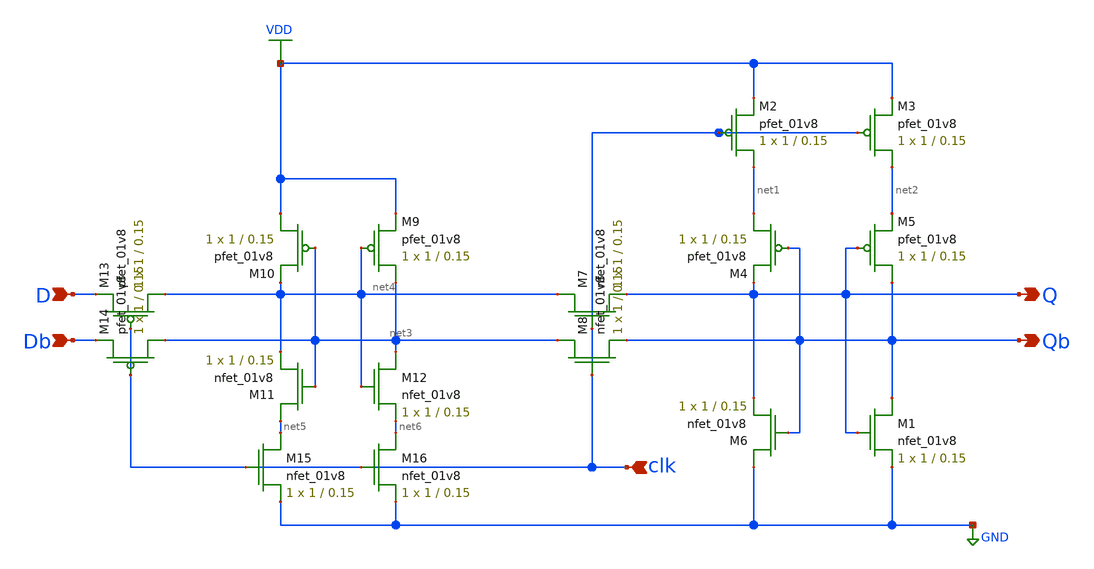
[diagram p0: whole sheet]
** sch_path: Miniproject2/dflipflop_lvs.sch
**.subckt dflipflop_lvs Q Db Qb D clk
*.opin Q
*.ipin Db
*.opin Qb
*.ipin D
*.ipin clk
XM1 Qb Q GND GND sky130_fd_pr__nfet_01v8 L=0.15 W=1 nf=1 ad='int((nf+1)/2) * W/nf * 0.29' as='int((nf+2)/2) * W/nf * 0.29'
+ pd='2*int((nf+1)/2) * (W/nf + 0.29)' ps='2*int((nf+2)/2) * (W/nf + 0.29)' nrd='0.29 / W' nrs='0.29 / W'
+ sa=0 sb=0 sd=0 mult=1 m=1
XM2 net1 clk VDD VDD sky130_fd_pr__pfet_01v8 L=0.15 W=1 nf=1 ad='int((nf+1)/2) * W/nf * 0.29' as='int((nf+2)/2) * W/nf * 0.29'
+ pd='2*int((nf+1)/2) * (W/nf + 0.29)' ps='2*int((nf+2)/2) * (W/nf + 0.29)' nrd='0.29 / W' nrs='0.29 / W'
+ sa=0 sb=0 sd=0 mult=1 m=1
XM3 net2 clk VDD VDD sky130_fd_pr__pfet_01v8 L=0.15 W=1 nf=1 ad='int((nf+1)/2) * W/nf * 0.29' as='int((nf+2)/2) * W/nf * 0.29'
+ pd='2*int((nf+1)/2) * (W/nf + 0.29)' ps='2*int((nf+2)/2) * (W/nf + 0.29)' nrd='0.29 / W' nrs='0.29 / W'
+ sa=0 sb=0 sd=0 mult=1 m=1
XM4 net1 Qb Q VDD sky130_fd_pr__pfet_01v8 L=0.15 W=1 nf=1 ad='int((nf+1)/2) * W/nf * 0.29' as='int((nf+2)/2) * W/nf * 0.29'
+ pd='2*int((nf+1)/2) * (W/nf + 0.29)' ps='2*int((nf+2)/2) * (W/nf + 0.29)' nrd='0.29 / W' nrs='0.29 / W'
+ sa=0 sb=0 sd=0 mult=1 m=1
XM5 Qb Q net2 VDD sky130_fd_pr__pfet_01v8 L=0.15 W=1 nf=1 ad='int((nf+1)/2) * W/nf * 0.29' as='int((nf+2)/2) * W/nf * 0.29'
+ pd='2*int((nf+1)/2) * (W/nf + 0.29)' ps='2*int((nf+2)/2) * (W/nf + 0.29)' nrd='0.29 / W' nrs='0.29 / W'
+ sa=0 sb=0 sd=0 mult=1 m=1
XM6 GND Qb Q GND sky130_fd_pr__nfet_01v8 L=0.15 W=1 nf=1 ad='int((nf+1)/2) * W/nf * 0.29' as='int((nf+2)/2) * W/nf * 0.29'
+ pd='2*int((nf+1)/2) * (W/nf + 0.29)' ps='2*int((nf+2)/2) * (W/nf + 0.29)' nrd='0.29 / W' nrs='0.29 / W'
+ sa=0 sb=0 sd=0 mult=1 m=1
XM7 net4 clk Q GND sky130_fd_pr__nfet_01v8 L=0.15 W=1 nf=1 ad='int((nf+1)/2) * W/nf * 0.29' as='int((nf+2)/2) * W/nf * 0.29'
+ pd='2*int((nf+1)/2) * (W/nf + 0.29)' ps='2*int((nf+2)/2) * (W/nf + 0.29)' nrd='0.29 / W' nrs='0.29 / W'
+ sa=0 sb=0 sd=0 mult=1 m=1
XM8 net3 clk Qb GND sky130_fd_pr__nfet_01v8 L=0.15 W=1 nf=1 ad='int((nf+1)/2) * W/nf * 0.29' as='int((nf+2)/2) * W/nf * 0.29'
+ pd='2*int((nf+1)/2) * (W/nf + 0.29)' ps='2*int((nf+2)/2) * (W/nf + 0.29)' nrd='0.29 / W' nrs='0.29 / W'
+ sa=0 sb=0 sd=0 mult=1 m=1
XM9 net3 net4 VDD VDD sky130_fd_pr__pfet_01v8 L=0.15 W=1 nf=1 ad='int((nf+1)/2) * W/nf * 0.29' as='int((nf+2)/2) * W/nf * 0.29'
+ pd='2*int((nf+1)/2) * (W/nf + 0.29)' ps='2*int((nf+2)/2) * (W/nf + 0.29)' nrd='0.29 / W' nrs='0.29 / W'
+ sa=0 sb=0 sd=0 mult=1 m=1
XM10 VDD net3 net4 VDD sky130_fd_pr__pfet_01v8 L=0.15 W=1 nf=1 ad='int((nf+1)/2) * W/nf * 0.29' as='int((nf+2)/2) * W/nf * 0.29'
+ pd='2*int((nf+1)/2) * (W/nf + 0.29)' ps='2*int((nf+2)/2) * (W/nf + 0.29)' nrd='0.29 / W' nrs='0.29 / W'
+ sa=0 sb=0 sd=0 mult=1 m=1
XM11 net5 net3 net4 GND sky130_fd_pr__nfet_01v8 L=0.15 W=1 nf=1 ad='int((nf+1)/2) * W/nf * 0.29' as='int((nf+2)/2) * W/nf * 0.29'
+ pd='2*int((nf+1)/2) * (W/nf + 0.29)' ps='2*int((nf+2)/2) * (W/nf + 0.29)' nrd='0.29 / W' nrs='0.29 / W'
+ sa=0 sb=0 sd=0 mult=1 m=1
XM12 net3 net4 net6 GND sky130_fd_pr__nfet_01v8 L=0.15 W=1 nf=1 ad='int((nf+1)/2) * W/nf * 0.29' as='int((nf+2)/2) * W/nf * 0.29'
+ pd='2*int((nf+1)/2) * (W/nf + 0.29)' ps='2*int((nf+2)/2) * (W/nf + 0.29)' nrd='0.29 / W' nrs='0.29 / W'
+ sa=0 sb=0 sd=0 mult=1 m=1
XM13 net4 clk D VDD sky130_fd_pr__pfet_01v8 L=0.15 W=1 nf=1 ad='int((nf+1)/2) * W/nf * 0.29' as='int((nf+2)/2) * W/nf * 0.29'
+ pd='2*int((nf+1)/2) * (W/nf + 0.29)' ps='2*int((nf+2)/2) * (W/nf + 0.29)' nrd='0.29 / W' nrs='0.29 / W'
+ sa=0 sb=0 sd=0 mult=1 m=1
XM14 net3 clk Db VDD sky130_fd_pr__pfet_01v8 L=0.15 W=1 nf=1 ad='int((nf+1)/2) * W/nf * 0.29' as='int((nf+2)/2) * W/nf * 0.29'
+ pd='2*int((nf+1)/2) * (W/nf + 0.29)' ps='2*int((nf+2)/2) * (W/nf + 0.29)' nrd='0.29 / W' nrs='0.29 / W'
+ sa=0 sb=0 sd=0 mult=1 m=1
XM15 net5 clk GND GND sky130_fd_pr__nfet_01v8 L=0.15 W=1 nf=1 ad='int((nf+1)/2) * W/nf * 0.29' as='int((nf+2)/2) * W/nf * 0.29'
+ pd='2*int((nf+1)/2) * (W/nf + 0.29)' ps='2*int((nf+2)/2) * (W/nf + 0.29)' nrd='0.29 / W' nrs='0.29 / W'
+ sa=0 sb=0 sd=0 mult=1 m=1
XM16 net6 clk GND GND sky130_fd_pr__nfet_01v8 L=0.15 W=1 nf=1 ad='int((nf+1)/2) * W/nf * 0.29' as='int((nf+2)/2) * W/nf * 0.29'
+ pd='2*int((nf+1)/2) * (W/nf + 0.29)' ps='2*int((nf+2)/2) * (W/nf + 0.29)' nrd='0.29 / W' nrs='0.29 / W'
+ sa=0 sb=0 sd=0 mult=1 m=1
**.ends
.GLOBAL VDD
.GLOBAL GND
.end
